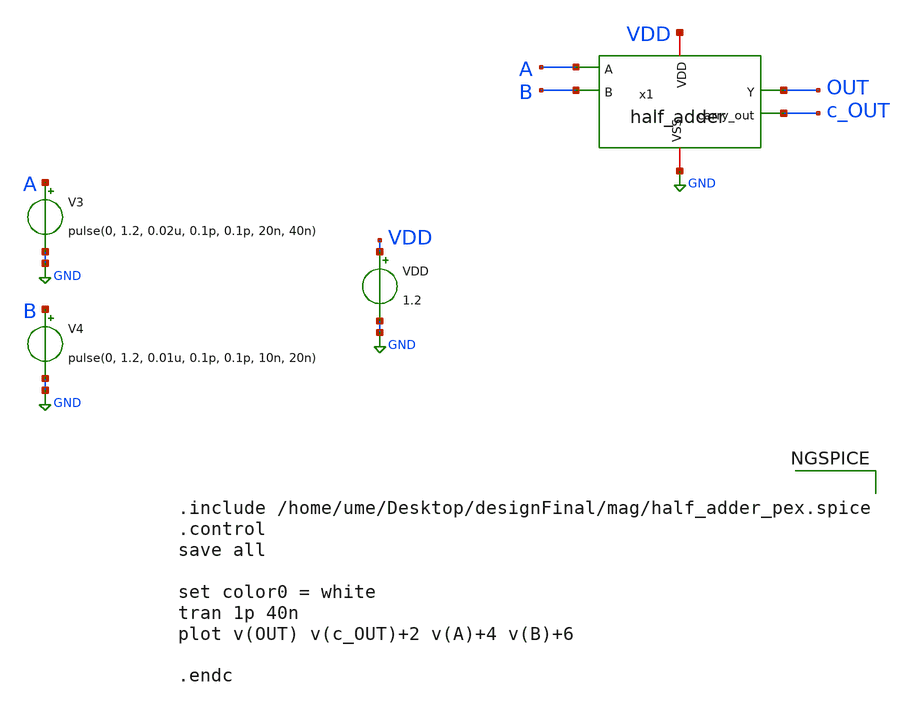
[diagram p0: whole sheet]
** sch_path: design/HALF_ADDER/xschem/half_adder_tb.sch
**.subckt half_adder_tb
VDD VDD GND 1.2
V3 A GND pulse(0, 1.2, 0.02u, 0.1p, 0.1p, 20n, 40n)
V4 B GND pulse(0, 1.2, 0.01u, 0.1p, 0.1p, 10n, 20n)
x1 A B OUT c_OUT VDD GND half_adder
**** begin user architecture code

** opencircuitdesign pdks install
.lib $::SKYWATER_MODELS/sky130.lib.spice tt_mm




.include /home/ume/Desktop/designFinal/mag/half_adder_pex.spice
.control
save all

set color0 = white
tran 1p 40n
plot v(OUT) v(c_OUT)+2 v(A)+4 v(B)+6

.endc

**** end user architecture code
**.ends
.GLOBAL GND
.end
